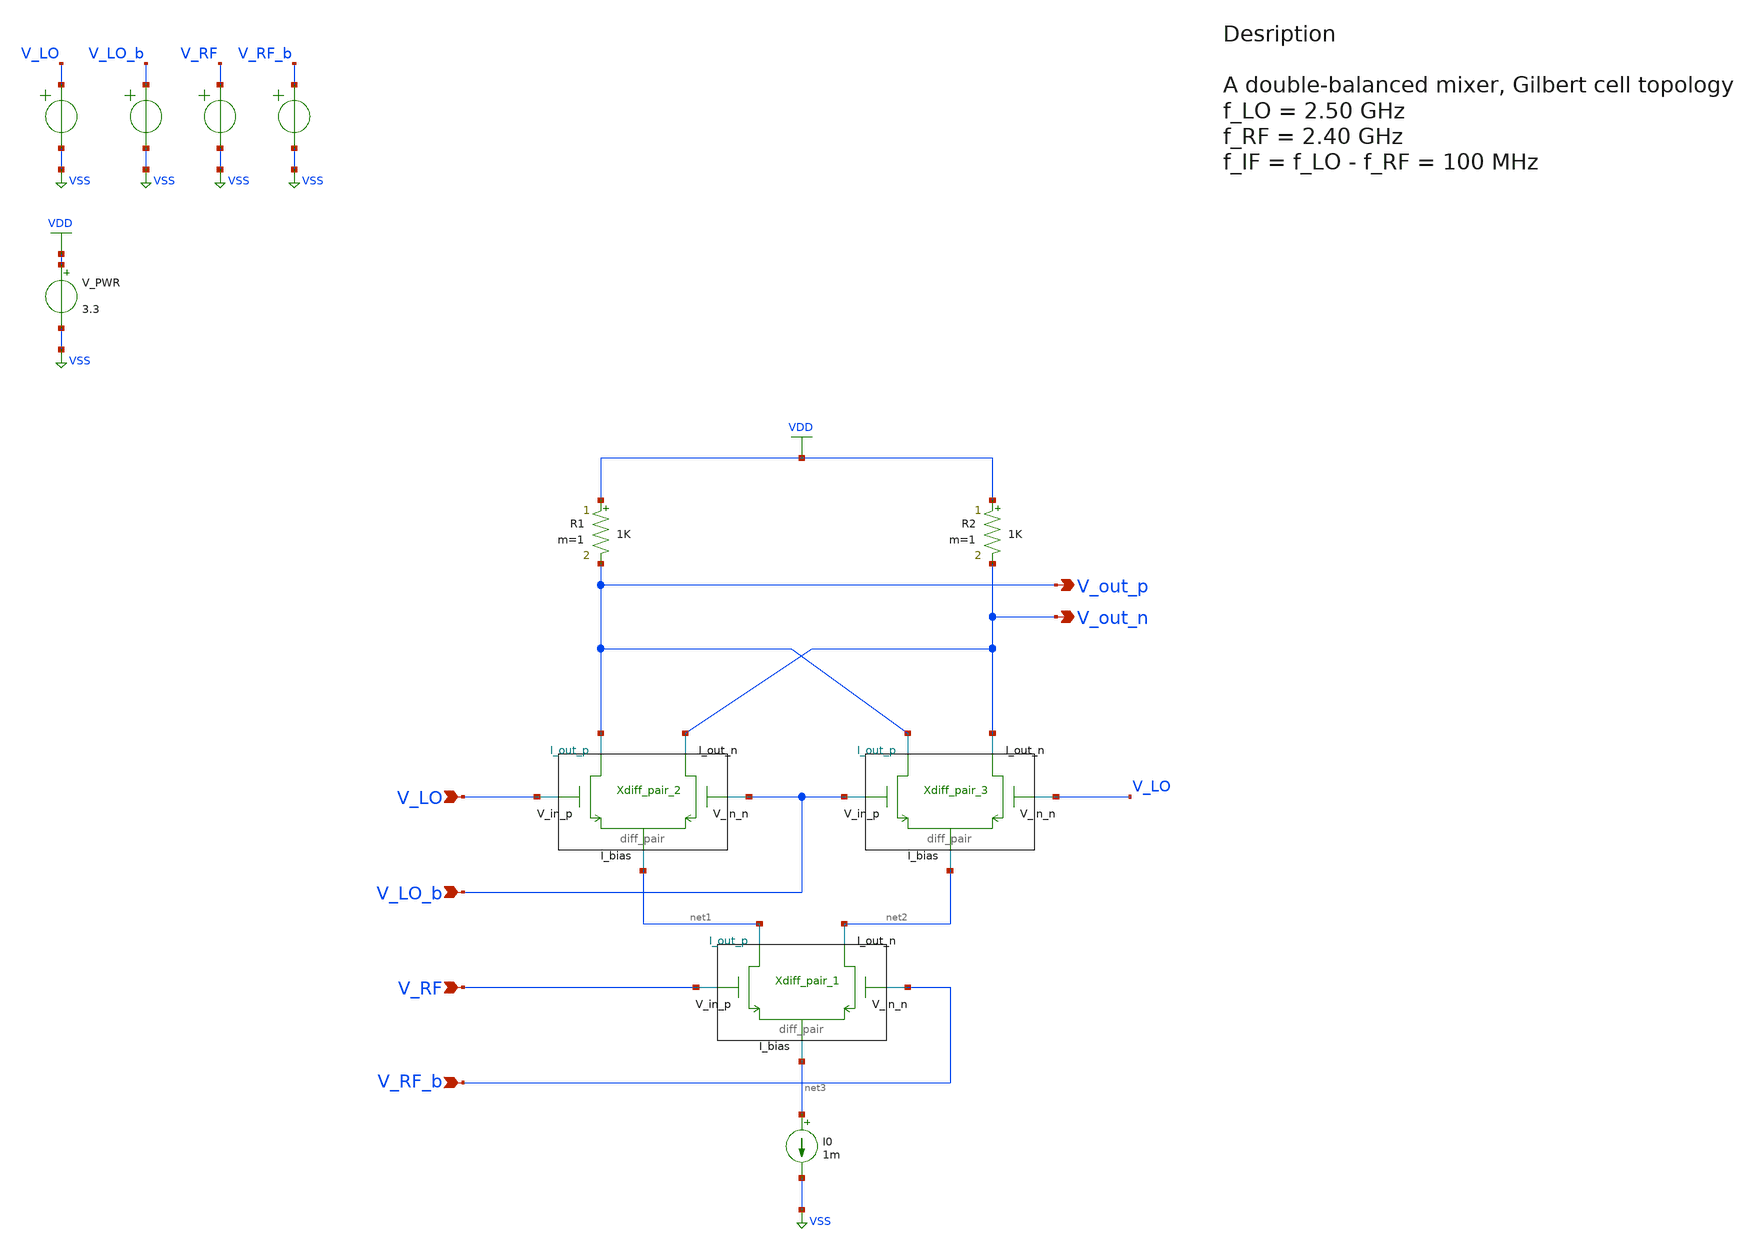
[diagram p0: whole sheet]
** sch_path: src/design_xsch/Gilbert_cell.sch
**.subckt Gilbert_cell V_LO V_LO_b V_RF V_RF_b V_out_p V_out_n
*.ipin V_LO
*.ipin V_LO_b
*.ipin V_RF
*.ipin V_RF_b
*.opin V_out_p
*.opin V_out_n
I0 net3 VSS 1m
E1 V_LO VSS VOL=' '1.5 + sin(time * 2.5 * 1e9)' '
E2 V_LO_b VSS VOL=' '1.5 - sin(time * 2.5 * 1e9)' '
E4 V_RF VSS VOL=' '1.5 + sin(time * 2.40 * 1e9)' '
E6 V_RF_b VSS VOL=' '1.5 - sin(time * 2.40 * 1e9)' '
Xdiff_pair_1 net2 net1 V_RF V_RF_b net3 VSS diff_pair W_neg=0.22u L_neg=0.28u W_pos=2u L_pos=0.28u
+ m=1
Xdiff_pair_2 V_out_n V_out_p V_LO V_LO_b net1 VSS diff_pair W_neg=0.22u L_neg=0.28u W_pos=0.22u
+ L_pos=0.28u m=1
Xdiff_pair_3 V_out_n V_out_p V_LO_b V_LO net2 VSS diff_pair W_neg=0.22u L_neg=0.28u W_pos=0.22u
+ L_pos=0.28u m=1
R1 VDD V_out_p 1K m=1
R2 VDD V_out_n 1K m=1
V_PWR VDD VSS 3.3
.save i(v_pwr)
**** begin user architecture code

.include $::180MCU_MODELS/design.ngspice
.lib $::180MCU_MODELS/sm141064.ngspice typical



.control

    save all

    * Define frequencies
    let f_lo = 2.5e9
    let f_rf = 2.4e9
    let f_if = 100e6

    * operating point
    op
    print all

    write Gilbert_cell.raw
    set appendwrite

    * Transient analysis to observe mixing operation
    tran 10p 20n

    * Calculate differential output for conversion gain measurement
    let v_out_diff = v(v_out_p) - v(v_out_n)
    let v_rf_diff = v(v_rf) - v(v_rf_b)

    * Extract IF component at 100MHz using FFT
    linearize v_out_diff v_rf_diff
    fft v_out_diff v_rf_diff

    * Measure conversion gain (power gain from RF to IF)
    let P_rf_in = mean(v_rf_diff*v_rf_diff)/1000  ; Assuming 1k input impedance
    let P_if_out = mean(v_out_diff*v_out_diff)/1000  ; Assuming 1k load
    let conversion_gain_db = 10*log10(P_if_out/P_rf_in)
    print conversion_gain_db

    write Gilbert_cell.raw

    * Two-tone test for IIP2 and IIP3 measurement
    * Reset sources for two-tone test
    alter @E4[vl] = '0.9 + 0.05*sin(2*pi*2.39e9*time) + 0.05*sin(2*pi*2.41e9*time)'
    alter @E6[vl] = '0.9 - 0.05*sin(2*pi*2.39e9*time) - 0.05*sin(2*pi*2.41e9*time)'

    tran 10p 50n

    * Linearize and perform FFT for intermodulation analysis
    linearize v_out_diff
    fft v_out_diff

    * Calculate fundamental and intermodulation products
    * IM2 products at f2-f1 = 20MHz and f2+f1 = 4.8GHz
    * IM3 products at 2*f1-f2 = 2.37GHz and 2*f2-f1 = 2.43GHz

    let fund_mag = abs(v_out_diff[100e6])  ; IF fundamental at 100MHz
    let im2_mag = abs(v_out_diff[20e6])    ; IM2 product at 20MHz
    let im3_mag = abs(v_out_diff[70e6])    ; IM3 product at 70MHz (2.4G-2.33G down-converted)

    * Calculate IIP2 and IIP3 (simplified calculation)
    let input_power_dbm = 10*log10(0.05*0.05/0.001) + 30  ; Input power in dBm
    let iip2_dbm = input_power_dbm + 10*log10(fund_mag*fund_mag/(im2_mag*im2_mag))/2
    let iip3_dbm = input_power_dbm + 10*log10(fund_mag*fund_mag/(im3_mag*im3_mag))*3/2

    print iip2_dbm iip3_dbm

    write Gilbert_cell.raw

    * Noise analysis for Noise Figure calculation
    * Reset to single tone for noise analysis
    alter @E4[vl] = '0.9 + 0.001*sin(2*pi*2.4e9*time)'  ; Small signal for noise
    alter @E6[vl] = '0.9 - 0.001*sin(2*pi*2.4e9*time)'

    noise v(v_out_p,v_out_n) E4 dec 10 1e6 1e9

    * Calculate Single Sideband Noise Figure
    * NF_SSB = NF_DSB + 3dB (for double sideband to single sideband conversion)
    setplot noise1
    let nf_dsb_db = 10*log10(onoise_total^2/inoise_total^2)
    let nf_ssb_db = nf_dsb_db + 3
    print nf_ssb_db

    * Summary of measurements
    echo
    echo *** GILBERT CELL MIXER PERFORMANCE SUMMARY ***
    echo Conversion Gain: $&conversion_gain_db dB
    echo IIP2: $&iip2_dbm dBm
    echo IIP3: $&iip3_dbm dBm
    echo Single Sideband Noise Figure: $&nf_ssb_db dB
    echo

    write Gilbert_cell.raw
.endc


**** end user architecture code
**.ends

* expanding   symbol:  /home/vasil/Downloads/SSCS_PICO_2025/src/design_xsch/diff_pair.sym # of
*+ pins=5
** sym_path: src/design_xsch/diff_pair.sym
** sch_path: src/design_xsch/diff_pair.sch
.subckt diff_pair I_out_n I_out_p V_in_p V_in_n I_bias VSSPIN  mult=1  W_neg=0.22u L_neg=0.28u
+ W_pos=0.22u L_pos=0.28u
*.ipin V_in_p
*.ipin V_in_n
*.iopin I_out_p
*.iopin I_out_n
*.iopin I_bias
XM1 I_out_p V_in_p I_bias VSS nfet_03v3 L=L_pos W=W_pos nf=1 ad='int((nf+1)/2) * W/nf * 0.18u' as='int((nf+2)/2) * W/nf * 0.18u'
+ pd='2*int((nf+1)/2) * (W/nf + 0.18u)' ps='2*int((nf+2)/2) * (W/nf + 0.18u)' nrd='0.18u / W' nrs='0.18u / W'
+ sa=0 sb=0 sd=0 m=mult
XM2 I_out_n V_in_n I_bias VSS nfet_03v3 L=L_neg W=W_neg nf=1 ad='int((nf+1)/2) * W/nf * 0.18u' as='int((nf+2)/2) * W/nf * 0.18u'
+ pd='2*int((nf+1)/2) * (W/nf + 0.18u)' ps='2*int((nf+2)/2) * (W/nf + 0.18u)' nrd='0.18u / W' nrs='0.18u / W'
+ sa=0 sb=0 sd=0 m=mult
.ends

.GLOBAL VSS
.GLOBAL VDD
.end
